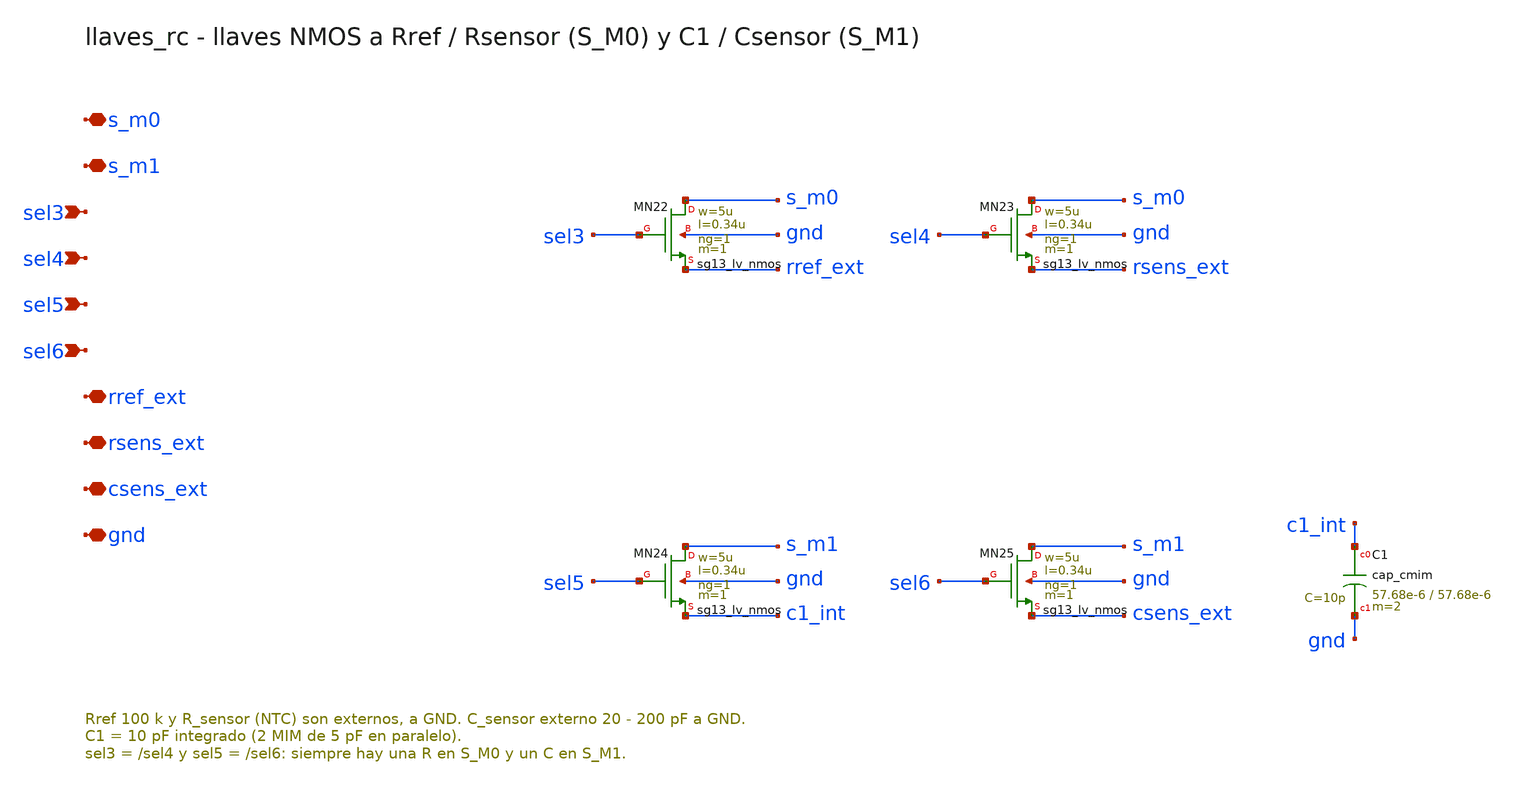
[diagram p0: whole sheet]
** sch_path: Enfoque_B/xschem/celdas/llaves_rc.sch
**.subckt llaves_rc s_m0 s_m1 sel3 sel4 sel5 sel6 rref_ext rsens_ext csens_ext gnd
*.iopin s_m0
*.iopin s_m1
*.ipin sel3
*.ipin sel4
*.ipin sel5
*.ipin sel6
*.iopin rref_ext
*.iopin rsens_ext
*.iopin csens_ext
*.iopin gnd
XMN22 s_m0 sel3 rref_ext gnd sg13_lv_nmos w=5u l=0.34u ng=1 m=1 mm_ok=1
XMN23 s_m0 sel4 rsens_ext gnd sg13_lv_nmos w=5u l=0.34u ng=1 m=1 mm_ok=1
XMN24 s_m1 sel5 c1_int gnd sg13_lv_nmos w=5u l=0.34u ng=1 m=1 mm_ok=1
XMN25 s_m1 sel6 csens_ext gnd sg13_lv_nmos w=5u l=0.34u ng=1 m=1 mm_ok=1
XC1 c1_int gnd cap_cmim w=57.68e-6 l=57.68e-6 m=2 mm_ok=1
**.ends
.end
